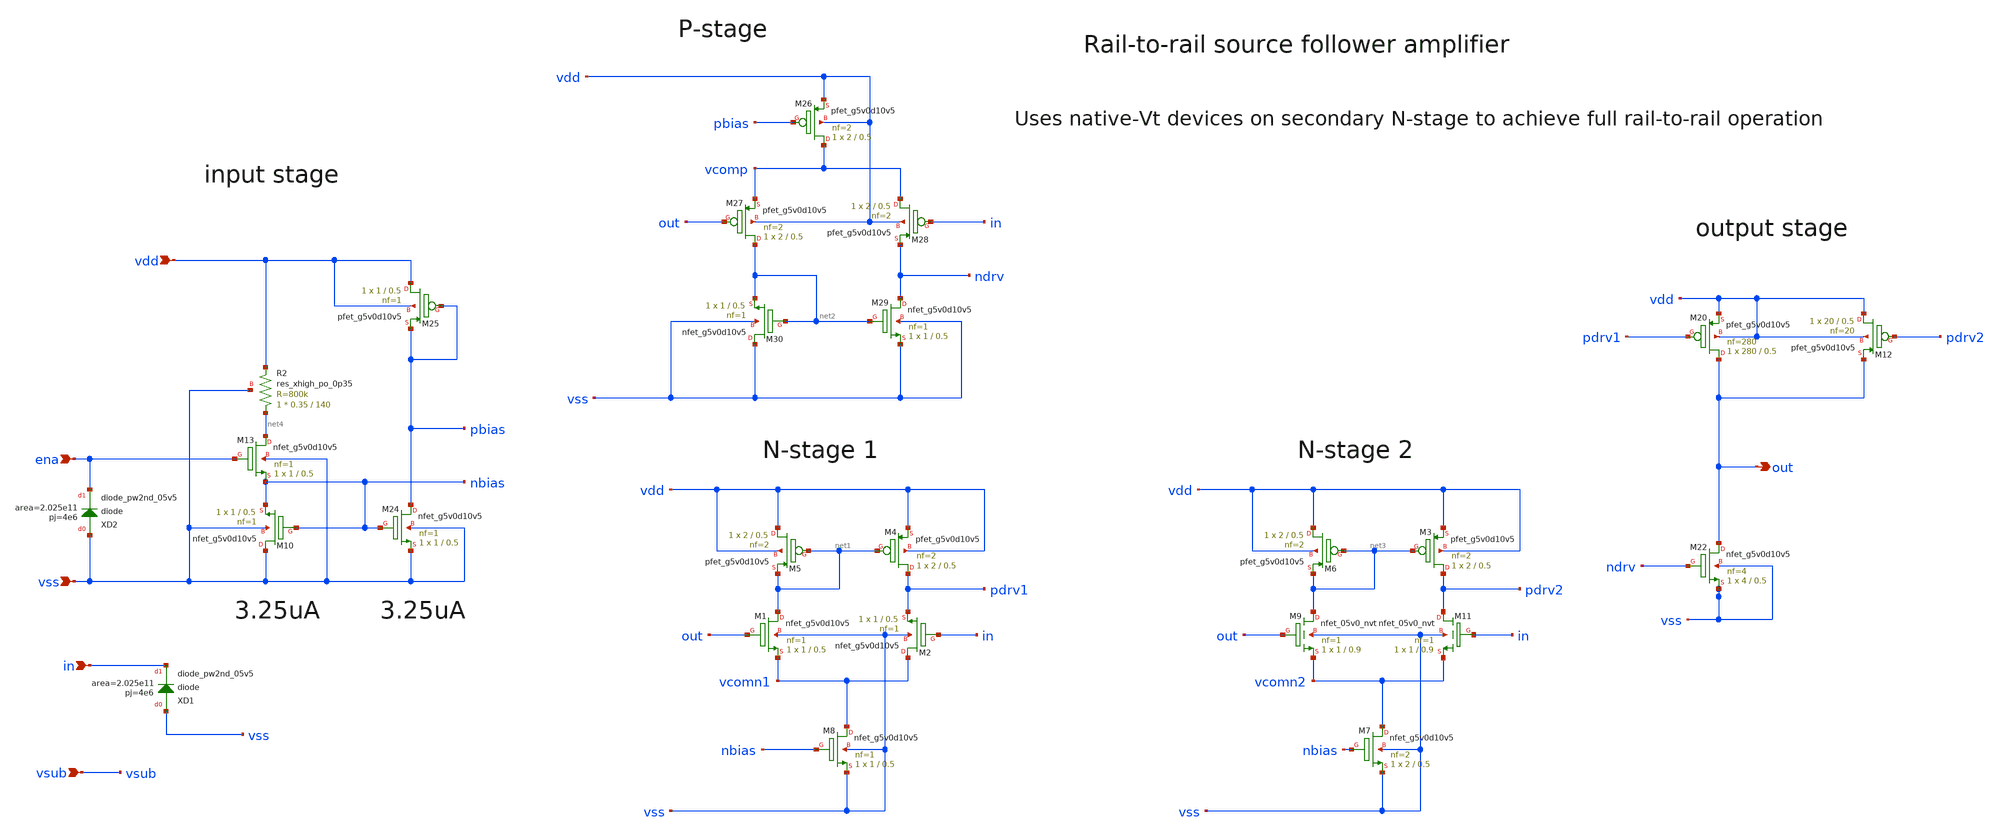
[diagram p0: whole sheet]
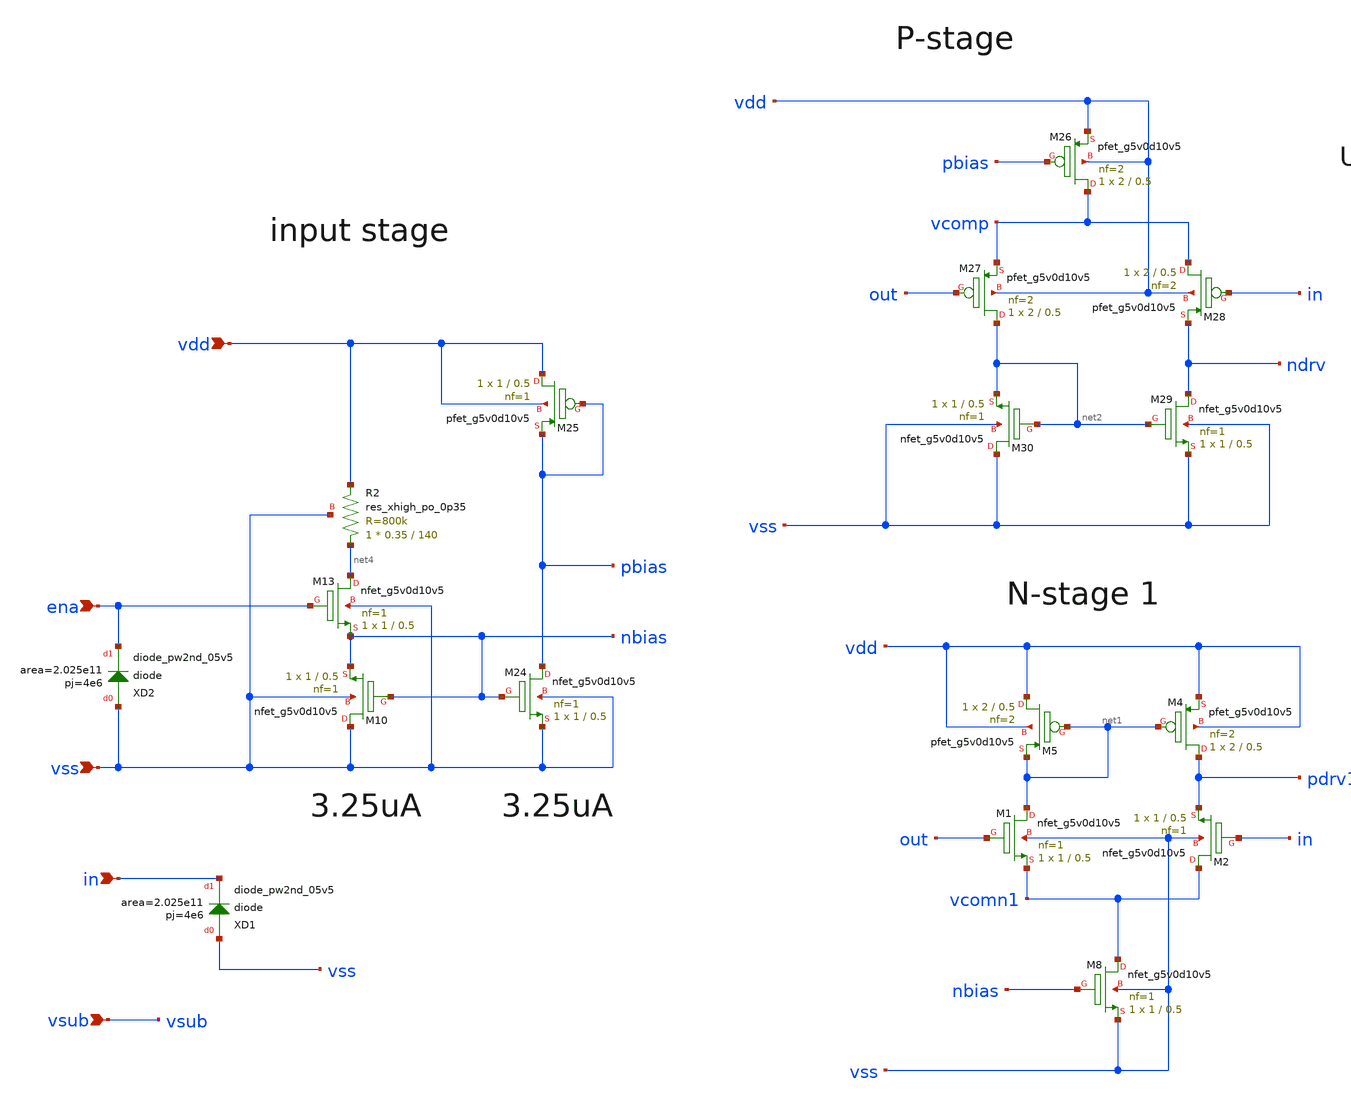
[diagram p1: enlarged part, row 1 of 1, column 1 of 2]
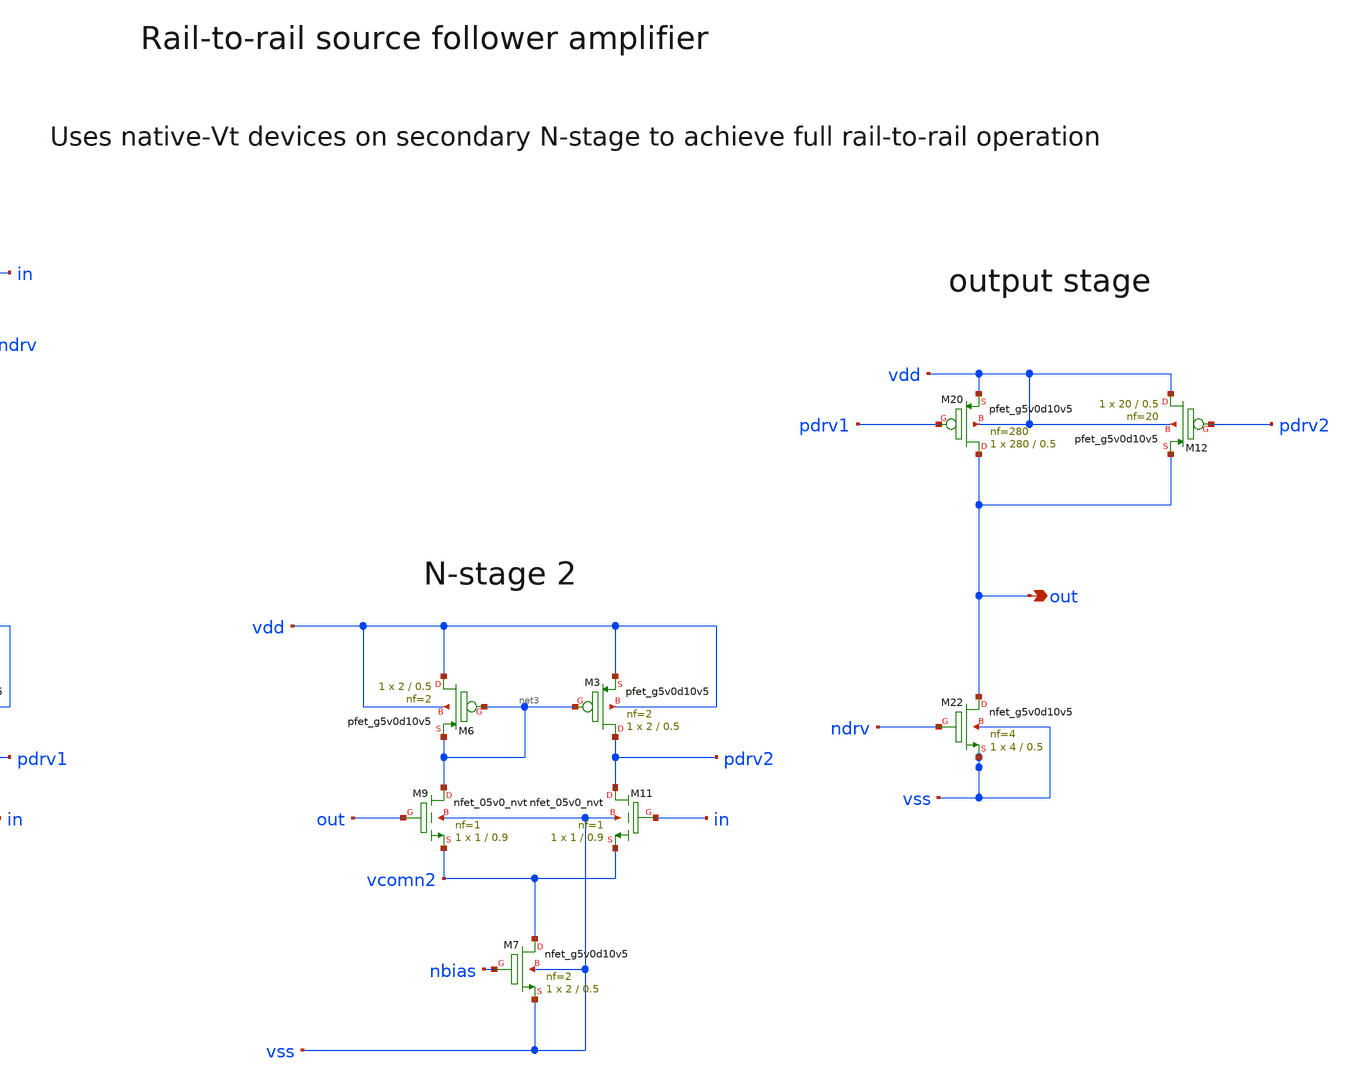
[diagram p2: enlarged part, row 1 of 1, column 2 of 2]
** sch_path: xschem/follower_amp.sch
**.subckt follower_amp in vdd vss out ena vsub
*.ipin in
*.ipin vdd
*.ipin vss
*.opin out
*.ipin ena
*.ipin vsub
XM4 pdrv1 net1 vdd vdd sky130_fd_pr__pfet_g5v0d10v5 L=0.5 W=2 nf=2 ad='int((nf+1)/2) * W/nf * 0.29' as='int((nf+2)/2) * W/nf * 0.29'
+ pd='2*int((nf+1)/2) * (W/nf + 0.29)' ps='2*int((nf+2)/2) * (W/nf + 0.29)' nrd='0.29 / W' nrs='0.29 / W'
+ sa=0 sb=0 sd=0 mult=1 m=1
XM5 vdd net1 net1 vdd sky130_fd_pr__pfet_g5v0d10v5 L=0.5 W=2 nf=2 ad='int((nf+1)/2) * W/nf * 0.29' as='int((nf+2)/2) * W/nf * 0.29'
+ pd='2*int((nf+1)/2) * (W/nf + 0.29)' ps='2*int((nf+2)/2) * (W/nf + 0.29)' nrd='0.29 / W' nrs='0.29 / W'
+ sa=0 sb=0 sd=0 mult=1 m=1
XM10 vss nbias nbias vss sky130_fd_pr__nfet_g5v0d10v5 L=0.5 W=1 nf=1 ad='int((nf+1)/2) * W/nf * 0.29'
+ as='int((nf+2)/2) * W/nf * 0.29' pd='2*int((nf+1)/2) * (W/nf + 0.29)' ps='2*int((nf+2)/2) * (W/nf + 0.29)'
+ nrd='0.29 / W' nrs='0.29 / W' sa=0 sb=0 sd=0 mult=1 m=1
XM20 out pdrv1 vdd vdd sky130_fd_pr__pfet_g5v0d10v5 L=0.5 W=280 nf=280 ad='int((nf+1)/2) * W/nf * 0.29'
+ as='int((nf+2)/2) * W/nf * 0.29' pd='2*int((nf+1)/2) * (W/nf + 0.29)' ps='2*int((nf+2)/2) * (W/nf + 0.29)'
+ nrd='0.29 / W' nrs='0.29 / W' sa=0 sb=0 sd=0 mult=1 m=1
XM22 out ndrv vss vss sky130_fd_pr__nfet_g5v0d10v5 L=0.5 W=4 nf=4 ad='int((nf+1)/2) * W/nf * 0.29' as='int((nf+2)/2) * W/nf * 0.29'
+ pd='2*int((nf+1)/2) * (W/nf + 0.29)' ps='2*int((nf+2)/2) * (W/nf + 0.29)' nrd='0.29 / W' nrs='0.29 / W'
+ sa=0 sb=0 sd=0 mult=1 m=1
XM24 pbias nbias vss vss sky130_fd_pr__nfet_g5v0d10v5 L=0.5 W=1 nf=1 ad='int((nf+1)/2) * W/nf * 0.29'
+ as='int((nf+2)/2) * W/nf * 0.29' pd='2*int((nf+1)/2) * (W/nf + 0.29)' ps='2*int((nf+2)/2) * (W/nf + 0.29)'
+ nrd='0.29 / W' nrs='0.29 / W' sa=0 sb=0 sd=0 mult=1 m=1
XM25 vdd pbias pbias vdd sky130_fd_pr__pfet_g5v0d10v5 L=0.5 W=1 nf=1 ad='int((nf+1)/2) * W/nf * 0.29'
+ as='int((nf+2)/2) * W/nf * 0.29' pd='2*int((nf+1)/2) * (W/nf + 0.29)' ps='2*int((nf+2)/2) * (W/nf + 0.29)'
+ nrd='0.29 / W' nrs='0.29 / W' sa=0 sb=0 sd=0 mult=1 m=1
XM26 vcomp pbias vdd vdd sky130_fd_pr__pfet_g5v0d10v5 L=0.5 W=2 nf=2 ad='int((nf+1)/2) * W/nf * 0.29'
+ as='int((nf+2)/2) * W/nf * 0.29' pd='2*int((nf+1)/2) * (W/nf + 0.29)' ps='2*int((nf+2)/2) * (W/nf + 0.29)'
+ nrd='0.29 / W' nrs='0.29 / W' sa=0 sb=0 sd=0 mult=1 m=1
XM27 net2 out vcomp vdd sky130_fd_pr__pfet_g5v0d10v5 L=0.5 W=2 nf=2 ad='int((nf+1)/2) * W/nf * 0.29'
+ as='int((nf+2)/2) * W/nf * 0.29' pd='2*int((nf+1)/2) * (W/nf + 0.29)' ps='2*int((nf+2)/2) * (W/nf + 0.29)'
+ nrd='0.29 / W' nrs='0.29 / W' sa=0 sb=0 sd=0 mult=1 m=1
XM28 vcomp in ndrv vdd sky130_fd_pr__pfet_g5v0d10v5 L=0.5 W=2 nf=2 ad='int((nf+1)/2) * W/nf * 0.29' as='int((nf+2)/2) * W/nf * 0.29'
+ pd='2*int((nf+1)/2) * (W/nf + 0.29)' ps='2*int((nf+2)/2) * (W/nf + 0.29)' nrd='0.29 / W' nrs='0.29 / W'
+ sa=0 sb=0 sd=0 mult=1 m=1
XM29 ndrv net2 vss vss sky130_fd_pr__nfet_g5v0d10v5 L=0.5 W=1 nf=1 ad='int((nf+1)/2) * W/nf * 0.29' as='int((nf+2)/2) * W/nf * 0.29'
+ pd='2*int((nf+1)/2) * (W/nf + 0.29)' ps='2*int((nf+2)/2) * (W/nf + 0.29)' nrd='0.29 / W' nrs='0.29 / W'
+ sa=0 sb=0 sd=0 mult=1 m=1
XM30 vss net2 net2 vss sky130_fd_pr__nfet_g5v0d10v5 L=0.5 W=1 nf=1 ad='int((nf+1)/2) * W/nf * 0.29' as='int((nf+2)/2) * W/nf * 0.29'
+ pd='2*int((nf+1)/2) * (W/nf + 0.29)' ps='2*int((nf+2)/2) * (W/nf + 0.29)' nrd='0.29 / W' nrs='0.29 / W'
+ sa=0 sb=0 sd=0 mult=1 m=1
XM1 net1 out vcomn1 vss sky130_fd_pr__nfet_g5v0d10v5 L=0.5 W=1 nf=1 ad='int((nf+1)/2) * W/nf * 0.29'
+ as='int((nf+2)/2) * W/nf * 0.29' pd='2*int((nf+1)/2) * (W/nf + 0.29)' ps='2*int((nf+2)/2) * (W/nf + 0.29)'
+ nrd='0.29 / W' nrs='0.29 / W' sa=0 sb=0 sd=0 mult=1 m=1
XM2 vcomn1 in pdrv1 vss sky130_fd_pr__nfet_g5v0d10v5 L=0.5 W=1 nf=1 ad='int((nf+1)/2) * W/nf * 0.29'
+ as='int((nf+2)/2) * W/nf * 0.29' pd='2*int((nf+1)/2) * (W/nf + 0.29)' ps='2*int((nf+2)/2) * (W/nf + 0.29)'
+ nrd='0.29 / W' nrs='0.29 / W' sa=0 sb=0 sd=0 mult=1 m=1
XM3 pdrv2 net3 vdd vdd sky130_fd_pr__pfet_g5v0d10v5 L=0.5 W=2 nf=2 ad='int((nf+1)/2) * W/nf * 0.29' as='int((nf+2)/2) * W/nf * 0.29'
+ pd='2*int((nf+1)/2) * (W/nf + 0.29)' ps='2*int((nf+2)/2) * (W/nf + 0.29)' nrd='0.29 / W' nrs='0.29 / W'
+ sa=0 sb=0 sd=0 mult=1 m=1
XM6 vdd net3 net3 vdd sky130_fd_pr__pfet_g5v0d10v5 L=0.5 W=2 nf=2 ad='int((nf+1)/2) * W/nf * 0.29' as='int((nf+2)/2) * W/nf * 0.29'
+ pd='2*int((nf+1)/2) * (W/nf + 0.29)' ps='2*int((nf+2)/2) * (W/nf + 0.29)' nrd='0.29 / W' nrs='0.29 / W'
+ sa=0 sb=0 sd=0 mult=1 m=1
XM7 vcomn2 nbias vss vss sky130_fd_pr__nfet_g5v0d10v5 L=0.5 W=2 nf=2 ad='int((nf+1)/2) * W/nf * 0.29'
+ as='int((nf+2)/2) * W/nf * 0.29' pd='2*int((nf+1)/2) * (W/nf + 0.29)' ps='2*int((nf+2)/2) * (W/nf + 0.29)'
+ nrd='0.29 / W' nrs='0.29 / W' sa=0 sb=0 sd=0 mult=1 m=1
XM12 vdd pdrv2 out vdd sky130_fd_pr__pfet_g5v0d10v5 L=0.5 W=20 nf=20 ad='int((nf+1)/2) * W/nf * 0.29'
+ as='int((nf+2)/2) * W/nf * 0.29' pd='2*int((nf+1)/2) * (W/nf + 0.29)' ps='2*int((nf+2)/2) * (W/nf + 0.29)'
+ nrd='0.29 / W' nrs='0.29 / W' sa=0 sb=0 sd=0 mult=1 m=1
XXD1 vss in sky130_fd_pr__diode_pw2nd_05v5 area=2.025e11 pj=4e6
XM13 net4 ena nbias vss sky130_fd_pr__nfet_g5v0d10v5 L=0.5 W=1 nf=1 ad='int((nf+1)/2) * W/nf * 0.29'
+ as='int((nf+2)/2) * W/nf * 0.29' pd='2*int((nf+1)/2) * (W/nf + 0.29)' ps='2*int((nf+2)/2) * (W/nf + 0.29)'
+ nrd='0.29 / W' nrs='0.29 / W' sa=0 sb=0 sd=0 mult=1 m=1
XXD2 vss ena sky130_fd_pr__diode_pw2nd_05v5 area=2.025e11 pj=4e6
XM11 pdrv2 in vcomn2 vss sky130_fd_pr__nfet_05v0_nvt L=0.9 W=1 nf=1 ad='int((nf+1)/2) * W/nf * 0.29'
+ as='int((nf+2)/2) * W/nf * 0.29' pd='2*int((nf+1)/2) * (W/nf + 0.29)' ps='2*int((nf+2)/2) * (W/nf + 0.29)'
+ nrd='0.29 / W' nrs='0.29 / W' sa=0 sb=0 sd=0 mult=1 m=1
XM9 net3 out vcomn2 vss sky130_fd_pr__nfet_05v0_nvt L=0.9 W=1 nf=1 ad='int((nf+1)/2) * W/nf * 0.29' as='int((nf+2)/2) * W/nf * 0.29'
+ pd='2*int((nf+1)/2) * (W/nf + 0.29)' ps='2*int((nf+2)/2) * (W/nf + 0.29)' nrd='0.29 / W' nrs='0.29 / W'
+ sa=0 sb=0 sd=0 mult=1 m=1
XM8 vcomn1 nbias vss vss sky130_fd_pr__nfet_g5v0d10v5 L=0.5 W=1 nf=1 ad='int((nf+1)/2) * W/nf * 0.29'
+ as='int((nf+2)/2) * W/nf * 0.29' pd='2*int((nf+1)/2) * (W/nf + 0.29)' ps='2*int((nf+2)/2) * (W/nf + 0.29)'
+ nrd='0.29 / W' nrs='0.29 / W' sa=0 sb=0 sd=0 mult=1 m=1
XR2 net4 vdd vss sky130_fd_pr__res_xhigh_po_0p35 L=140 mult=1 m=1
**.ends
.end
